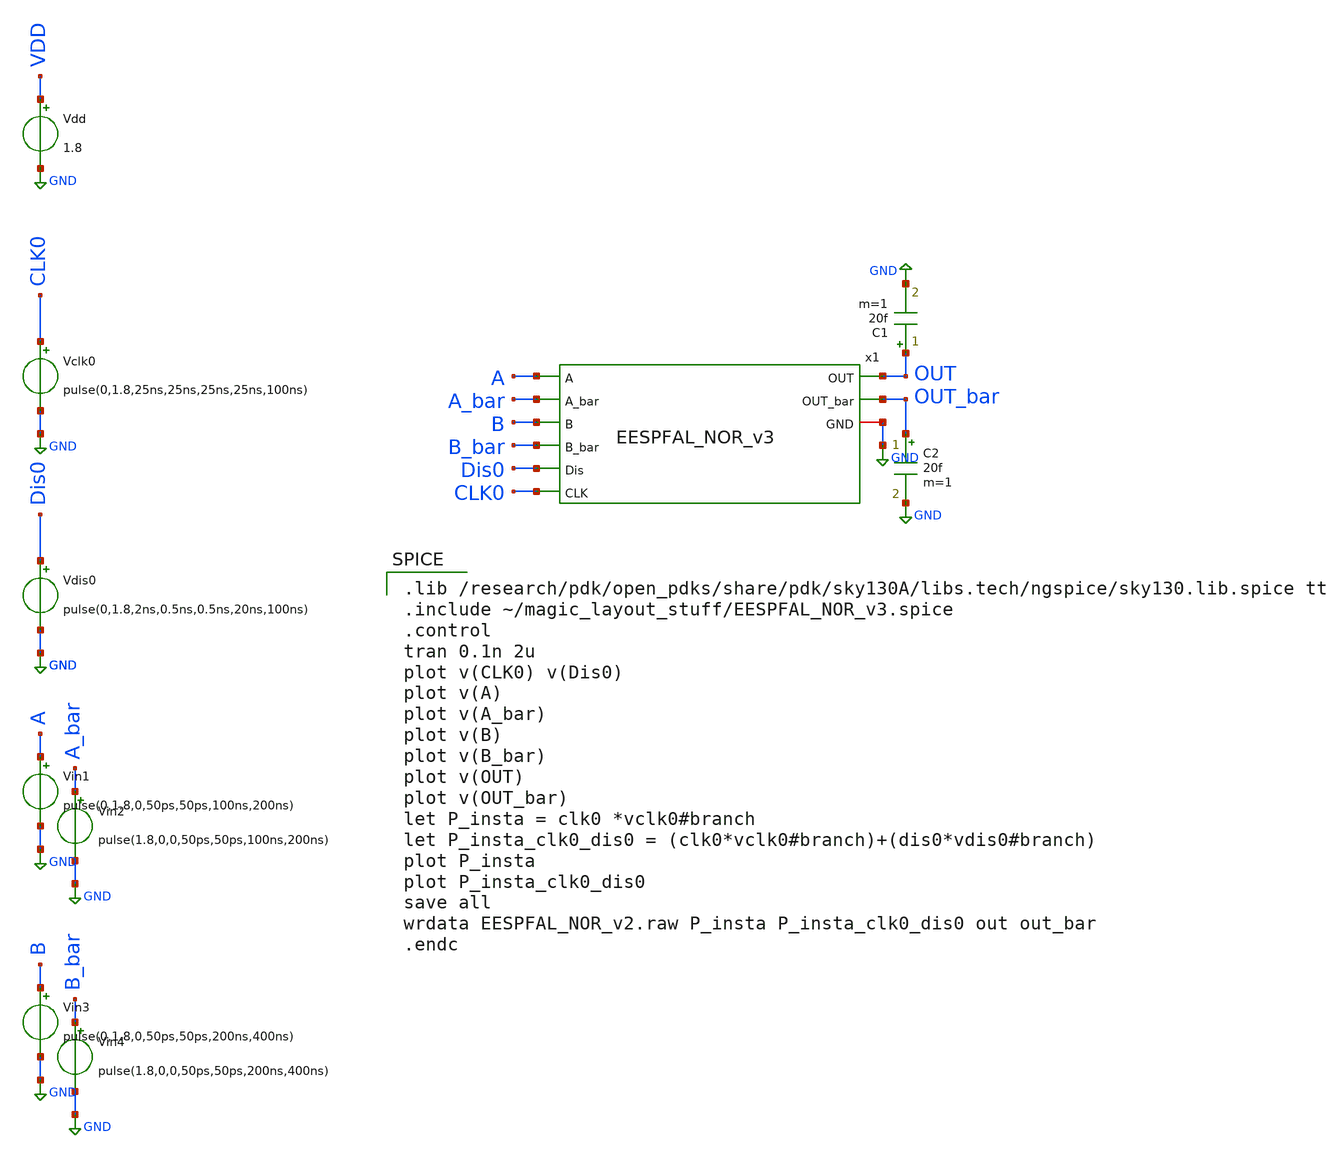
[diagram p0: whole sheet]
** sch_path: skywater_stuff/EESPFAL_NOR_sim.sch
**.subckt EESPFAL_NOR_sim
Vclk0 CLK0 GND pulse(0,1.8,25ns,25ns,25ns,25ns,100ns)
Vin1 A GND pulse(0,1.8,0,50ps,50ps,100ns,200ns)
Vin2 A_bar GND pulse(1.8,0,0,50ps,50ps,100ns,200ns)
Vdis0 Dis0 GND pulse(0,1.8,2ns,0.5ns,0.5ns,20ns,100ns)
Vdd VDD GND 1.8
Vin3 B GND pulse(0,1.8,0,50ps,50ps,200ns,400ns)
Vin4 B_bar GND pulse(1.8,0,0,50ps,50ps,200ns,400ns)
C1 OUT GND 20f m=1
C2 OUT_bar GND 20f m=1
x1 A A_bar B B_bar OUT OUT_bar Dis0 GND CLK0 EESPFAL_NOR_v3
**** begin user architecture code

.lib /research/pdk/open_pdks/share/pdk/sky130A/libs.tech/ngspice/sky130.lib.spice tt
.include ~/magic_layout_stuff/EESPFAL_NOR_v3.spice
.control
tran 0.1n 2u
plot v(CLK0) v(Dis0)
plot v(A)
plot v(A_bar)
plot v(B)
plot v(B_bar)
plot v(OUT)
plot v(OUT_bar)
let P_insta = clk0 *vclk0#branch
let P_insta_clk0_dis0 = (clk0*vclk0#branch)+(dis0*vdis0#branch)
plot P_insta
plot P_insta_clk0_dis0
save all
wrdata EESPFAL_NOR_v2.raw P_insta P_insta_clk0_dis0 out out_bar
.endc


**** end user architecture code
**.ends
.GLOBAL GND
.end
